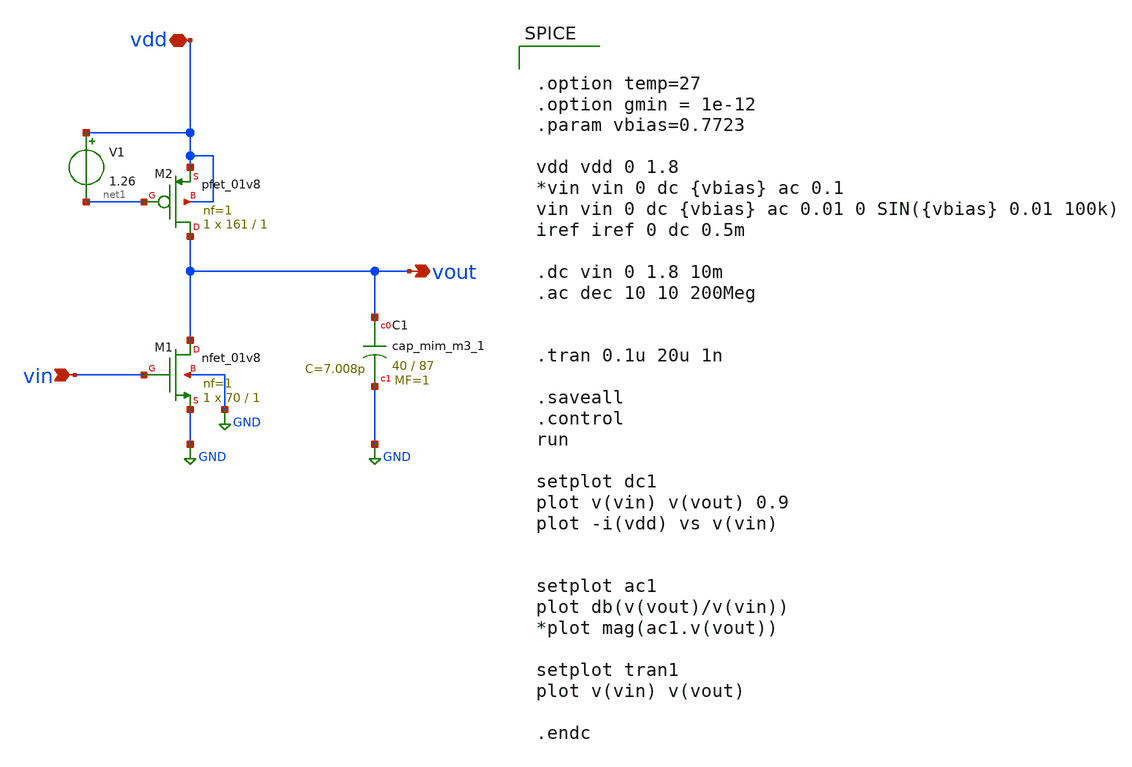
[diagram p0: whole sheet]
** sch_path: src/CS_CurrentS.sch
**.subckt CS_CurrentS vin vout vdd
*.ipin vin
*.opin vout
*.iopin vdd
XC1 vout GND sky130_fd_pr__cap_mim_m3_1 W=40 L=87 MF=1 m=1
V1 vdd net1 1.26
XM2 vout net1 vdd vdd sky130_fd_pr__pfet_01v8 L=1 W=161 nf=1 ad='int((nf+1)/2) * W/nf * 0.29' as='int((nf+2)/2) * W/nf * 0.29'
+ pd='2*int((nf+1)/2) * (W/nf + 0.29)' ps='2*int((nf+2)/2) * (W/nf + 0.29)' nrd='0.29 / W' nrs='0.29 / W'
+ sa=0 sb=0 sd=0 mult=1 m=1
XM1 vout vin GND GND sky130_fd_pr__nfet_01v8 L=1 W=70 nf=1 ad='int((nf+1)/2) * W/nf * 0.29' as='int((nf+2)/2) * W/nf * 0.29'
+ pd='2*int((nf+1)/2) * (W/nf + 0.29)' ps='2*int((nf+2)/2) * (W/nf + 0.29)' nrd='0.29 / W' nrs='0.29 / W'
+ sa=0 sb=0 sd=0 mult=1 m=1
**** begin user architecture code

** opencircuitdesign pdks install
.lib $::SKYWATER_MODELS/sky130.lib.spice tt




.option temp=27
.option gmin = 1e-12
.param vbias=0.7723

vdd vdd 0 1.8
*vin vin 0 dc {vbias} ac 0.1
vin vin 0 dc {vbias} ac 0.01 0 SIN({vbias} 0.01 100k)
iref iref 0 dc 0.5m

.dc vin 0 1.8 10m
.ac dec 10 10 200Meg


.tran 0.1u 20u 1n

.saveall
.control
run

setplot dc1
plot v(vin) v(vout) 0.9
plot -i(vdd) vs v(vin)


setplot ac1
plot db(v(vout)/v(vin))
*plot mag(ac1.v(vout))

setplot tran1
plot v(vin) v(vout)

.endc


**** end user architecture code
**.ends
.GLOBAL GND
.end
